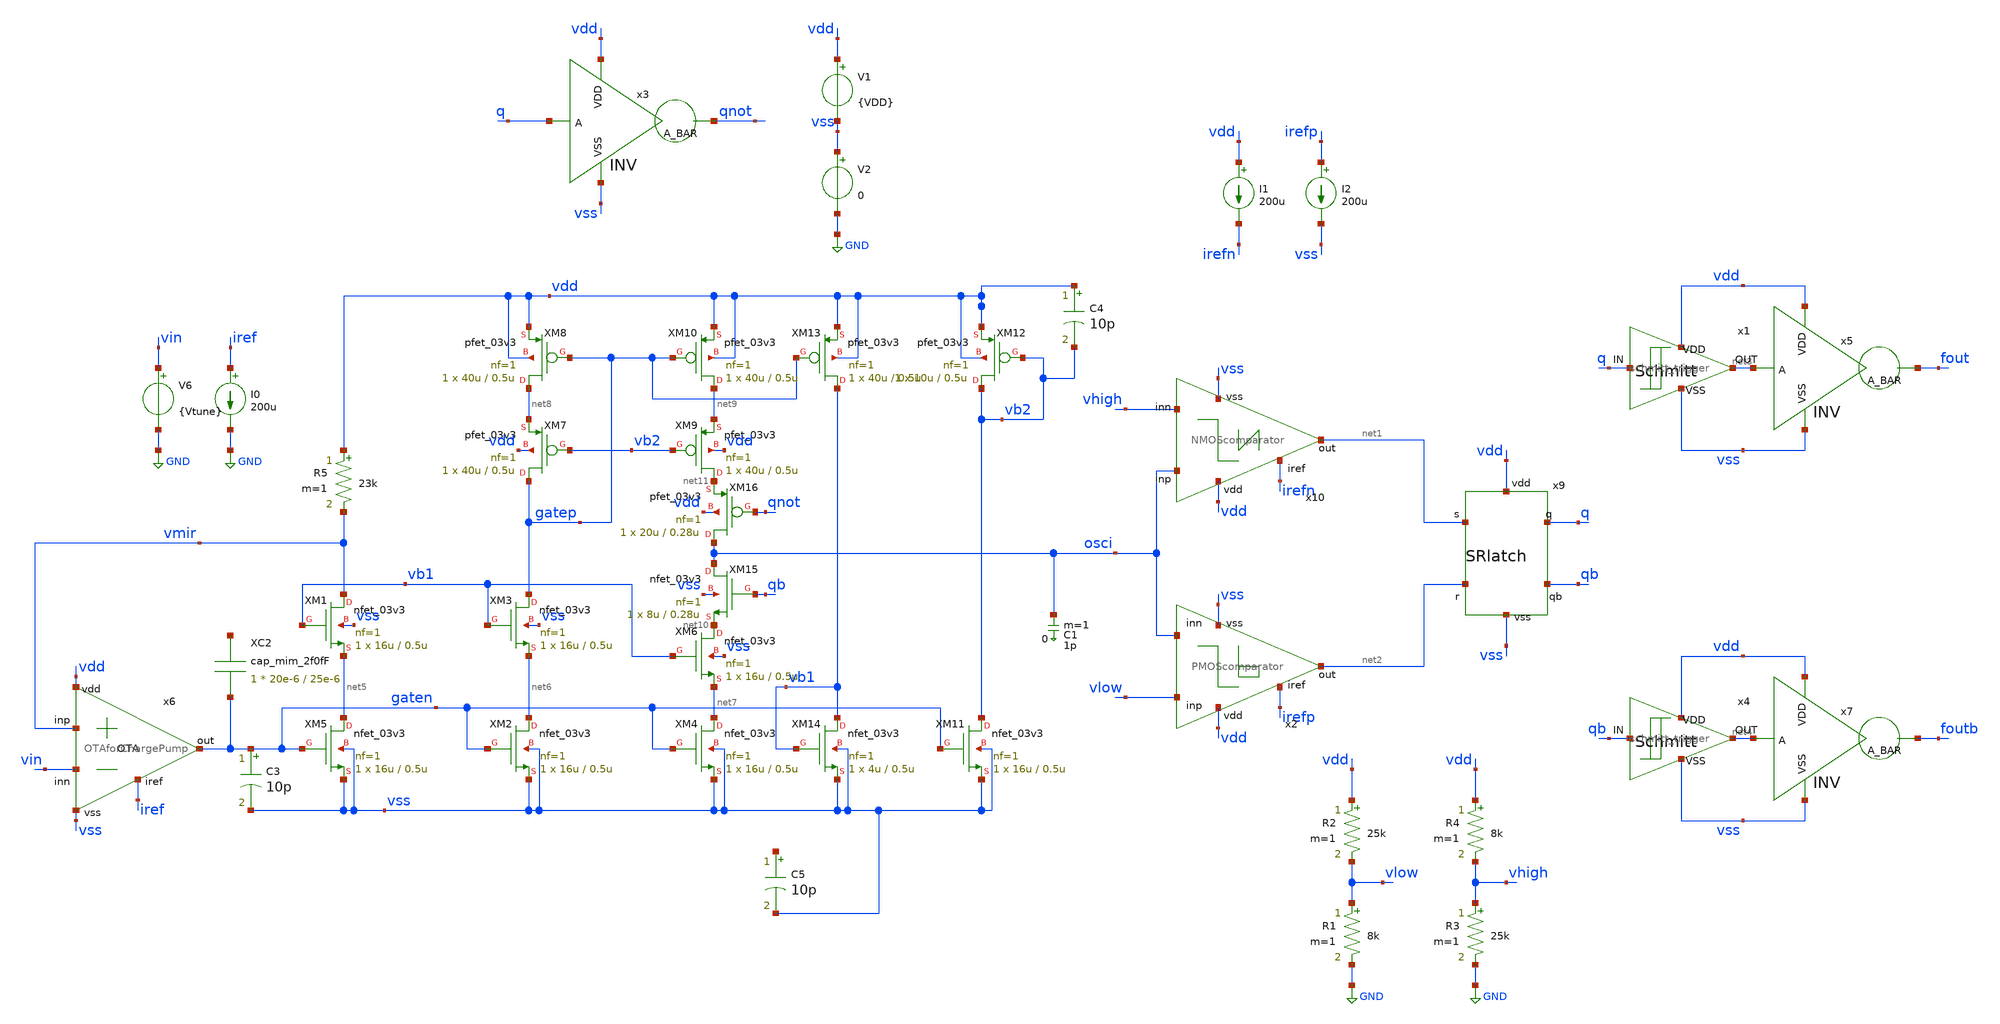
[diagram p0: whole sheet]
** sch_path: designs/libs/qw_core_analog/RVCO_0812/RVCO_0812.sch
**.subckt RVCO_0812
V1 vdd vss {VDD}
V2 vss GND 0
C1 osci 0 1p m=1
I1 vdd irefn 200u
I2 irefp vss 200u
R1 vlow GND 8k m=1
R2 vdd vlow 25k m=1
R3 vhigh GND 25k m=1
R4 vdd vhigh 8k m=1
x9 vdd net1 q qb net2 vss SRlatch
x2 vdd irefp vlow net2 osci vss PMOScomparator
x10 vdd osci net1 vhigh irefn vss NMOScomparator
x3 vdd q qnot vss INV
x1 q net3 vdd vss schmitt_trigger
x4 qb net4 vdd vss schmitt_trigger
x5 vdd net3 fout vss INV
x7 vdd net4 foutb vss INV
x6 vdd iref vmir vin gaten vss OTAforChargePump
XM5 net5 gaten vss vss nfet_03v3 L=0.5u W=16u nf=1 ad='int((nf+1)/2) * W/nf * 0.18u' as='int((nf+2)/2) * W/nf * 0.18u'
+ pd='2*int((nf+1)/2) * (W/nf + 0.18u)' ps='2*int((nf+2)/2) * (W/nf + 0.18u)' nrd='0.18u / W' nrs='0.18u / W'
+ sa=0 sb=0 sd=0 m=1
XM1 vmir vb1 net5 vss nfet_03v3 L=0.5u W=16u nf=1 ad='int((nf+1)/2) * W/nf * 0.18u' as='int((nf+2)/2) * W/nf * 0.18u'
+ pd='2*int((nf+1)/2) * (W/nf + 0.18u)' ps='2*int((nf+2)/2) * (W/nf + 0.18u)' nrd='0.18u / W' nrs='0.18u / W'
+ sa=0 sb=0 sd=0 m=1
XM2 net6 gaten vss vss nfet_03v3 L=0.5u W=16u nf=1 ad='int((nf+1)/2) * W/nf * 0.18u' as='int((nf+2)/2) * W/nf * 0.18u'
+ pd='2*int((nf+1)/2) * (W/nf + 0.18u)' ps='2*int((nf+2)/2) * (W/nf + 0.18u)' nrd='0.18u / W' nrs='0.18u / W'
+ sa=0 sb=0 sd=0 m=1
XM3 gatep vb1 net6 vss nfet_03v3 L=0.5u W=16u nf=1 ad='int((nf+1)/2) * W/nf * 0.18u' as='int((nf+2)/2) * W/nf * 0.18u'
+ pd='2*int((nf+1)/2) * (W/nf + 0.18u)' ps='2*int((nf+2)/2) * (W/nf + 0.18u)' nrd='0.18u / W' nrs='0.18u / W'
+ sa=0 sb=0 sd=0 m=1
XM4 net7 gaten vss vss nfet_03v3 L=0.5u W=16u nf=1 ad='int((nf+1)/2) * W/nf * 0.18u' as='int((nf+2)/2) * W/nf * 0.18u'
+ pd='2*int((nf+1)/2) * (W/nf + 0.18u)' ps='2*int((nf+2)/2) * (W/nf + 0.18u)' nrd='0.18u / W' nrs='0.18u / W'
+ sa=0 sb=0 sd=0 m=1
XM6 net10 vb1 net7 vss nfet_03v3 L=0.5u W=16u nf=1 ad='int((nf+1)/2) * W/nf * 0.18u' as='int((nf+2)/2) * W/nf * 0.18u'
+ pd='2*int((nf+1)/2) * (W/nf + 0.18u)' ps='2*int((nf+2)/2) * (W/nf + 0.18u)' nrd='0.18u / W' nrs='0.18u / W'
+ sa=0 sb=0 sd=0 m=1
XM7 gatep vb2 net8 vdd pfet_03v3 L=0.5u W=40u nf=1 ad='int((nf+1)/2) * W/nf * 0.18u' as='int((nf+2)/2) * W/nf * 0.18u'
+ pd='2*int((nf+1)/2) * (W/nf + 0.18u)' ps='2*int((nf+2)/2) * (W/nf + 0.18u)' nrd='0.18u / W' nrs='0.18u / W'
+ sa=0 sb=0 sd=0 m=1
XM8 net8 gatep vdd vdd pfet_03v3 L=0.5u W=40u nf=1 ad='int((nf+1)/2) * W/nf * 0.18u' as='int((nf+2)/2) * W/nf * 0.18u'
+ pd='2*int((nf+1)/2) * (W/nf + 0.18u)' ps='2*int((nf+2)/2) * (W/nf + 0.18u)' nrd='0.18u / W' nrs='0.18u / W'
+ sa=0 sb=0 sd=0 m=1
XM9 net11 vb2 net9 vdd pfet_03v3 L=0.5u W=40u nf=1 ad='int((nf+1)/2) * W/nf * 0.18u' as='int((nf+2)/2) * W/nf * 0.18u'
+ pd='2*int((nf+1)/2) * (W/nf + 0.18u)' ps='2*int((nf+2)/2) * (W/nf + 0.18u)' nrd='0.18u / W' nrs='0.18u / W'
+ sa=0 sb=0 sd=0 m=1
XM10 net9 gatep vdd vdd pfet_03v3 L=0.5u W=40u nf=1 ad='int((nf+1)/2) * W/nf * 0.18u' as='int((nf+2)/2) * W/nf * 0.18u'
+ pd='2*int((nf+1)/2) * (W/nf + 0.18u)' ps='2*int((nf+2)/2) * (W/nf + 0.18u)' nrd='0.18u / W' nrs='0.18u / W'
+ sa=0 sb=0 sd=0 m=1
R5 vdd vmir 23k m=1
XM11 vb2 gaten vss vss nfet_03v3 L=0.5u W=16u nf=1 ad='int((nf+1)/2) * W/nf * 0.18u' as='int((nf+2)/2) * W/nf * 0.18u'
+ pd='2*int((nf+1)/2) * (W/nf + 0.18u)' ps='2*int((nf+2)/2) * (W/nf + 0.18u)' nrd='0.18u / W' nrs='0.18u / W'
+ sa=0 sb=0 sd=0 m=1
XM12 vb2 vb2 vdd vdd pfet_03v3 L=0.5u W=10u nf=1 ad='int((nf+1)/2) * W/nf * 0.18u' as='int((nf+2)/2) * W/nf * 0.18u'
+ pd='2*int((nf+1)/2) * (W/nf + 0.18u)' ps='2*int((nf+2)/2) * (W/nf + 0.18u)' nrd='0.18u / W' nrs='0.18u / W'
+ sa=0 sb=0 sd=0 m=1
XM13 vb1 gatep vdd vdd pfet_03v3 L=0.5u W=40u nf=1 ad='int((nf+1)/2) * W/nf * 0.18u' as='int((nf+2)/2) * W/nf * 0.18u'
+ pd='2*int((nf+1)/2) * (W/nf + 0.18u)' ps='2*int((nf+2)/2) * (W/nf + 0.18u)' nrd='0.18u / W' nrs='0.18u / W'
+ sa=0 sb=0 sd=0 m=1
XM14 vb1 vb1 vss vss nfet_03v3 L=0.5u W=4u nf=1 ad='int((nf+1)/2) * W/nf * 0.18u' as='int((nf+2)/2) * W/nf * 0.18u'
+ pd='2*int((nf+1)/2) * (W/nf + 0.18u)' ps='2*int((nf+2)/2) * (W/nf + 0.18u)' nrd='0.18u / W' nrs='0.18u / W'
+ sa=0 sb=0 sd=0 m=1
XM15 osci qb net10 vss nfet_03v3 L=0.28u W=8u nf=1 ad='int((nf+1)/2) * W/nf * 0.18u' as='int((nf+2)/2) * W/nf * 0.18u'
+ pd='2*int((nf+1)/2) * (W/nf + 0.18u)' ps='2*int((nf+2)/2) * (W/nf + 0.18u)' nrd='0.18u / W' nrs='0.18u / W'
+ sa=0 sb=0 sd=0 m=1
XM16 osci qnot net11 vdd pfet_03v3 L=0.28u W=20u nf=1 ad='int((nf+1)/2) * W/nf * 0.18u' as='int((nf+2)/2) * W/nf * 0.18u'
+ pd='2*int((nf+1)/2) * (W/nf + 0.18u)' ps='2*int((nf+2)/2) * (W/nf + 0.18u)' nrd='0.18u / W' nrs='0.18u / W'
+ sa=0 sb=0 sd=0 m=1
V6 vin GND {Vtune}
I0 iref GND 200u
XC2 net12 gaten cap_mim_2f0fF c_width=20e-6 c_length=25e-6 m=1
C3 gaten vss 10p m=1
C4 vdd vb2 10p m=1
C5 net13 vss 10p m=1
**** begin user architecture code


* .param par_vth=0 par_k=0 par_l=0 par_w=0 par_leff=0 par_weff=0 p_sqrtarea=0 var_k=0 var_vth=0
.param VDD = 3.3 Vtune = {VDD/2}
.control
save all

**OP
**show all > op.log
**show all

** Source settings
**alter @V5[PULSE] = [ 1.64 1.66 20n 0.1n 0.1n 19.98n 40n 0 ]
**alter @V4[PULSE] = [ 1.66 1.64 20n 0.1n 0.1n 19.98n 40n 0 ]
**alter @V3[PULSE] = [ 0 3.3 10n 0.01n 0.01n 9.98n 20n 0 ]
**alter @V4[PULSE] = [ 0 3.3 50u 0.1u 0.1u 49.8u 100u 0 ]
alter @V1[PULSE] = [ 0 3.3 5n 1n 1n 49.998u 100u 0 ]

** Simulation settings

tran .1n 10u

write RVCO_0812.raw
.endc



.include $::180MCU_MODELS/design.ngspice
.lib $::180MCU_MODELS/sm141064.ngspice typical
.lib $::180MCU_MODELS/sm141064.ngspice cap_mim
.lib $::180MCU_MODELS/sm141064.ngspice res_typical
.lib $::180MCU_MODELS/sm141064.ngspice moscap_typical
.lib $::180MCU_MODELS/sm141064.ngspice mimcap_typical
* .lib $::180MCU_MODELS/sm141064.ngspice res_statistical

**** end user architecture code
**.ends
.GLOBAL GND
.end
